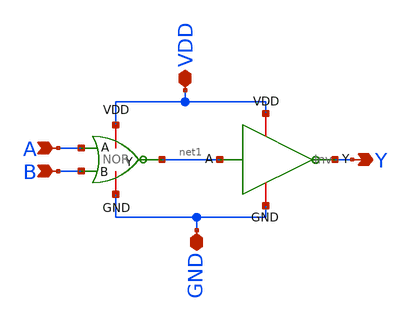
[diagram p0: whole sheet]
** sch_path: FinalProj/OR.sch
**.subckt OR VDD GND A B Y
*.iopin VDD
*.iopin GND
*.ipin A
*.ipin B
*.opin Y
x1 VDD B net1 A GND NOR
x2 VDD net1 Y GND Inv
**.ends

* expanding   symbol:  workspace/FinalProj/NOR.sym # of pins=5
** sym_path: FinalProj/NOR.sym
** sch_path: FinalProj/NOR.sch
.subckt NOR VDD B Y A GND
*.ipin B
*.ipin A
*.iopin GND
*.iopin VDD
*.opin Y
XM1 net1 A VDD VDD sky130_fd_pr__pfet_01v8 L=0.5 W=2 nf=1 ad='int((nf+1)/2) * W/nf * 0.29' as='int((nf+2)/2) * W/nf * 0.29'
+ pd='2*int((nf+1)/2) * (W/nf + 0.29)' ps='2*int((nf+2)/2) * (W/nf + 0.29)' nrd='0.29 / W' nrs='0.29 / W'
+ sa=0 sb=0 sd=0 mult=1 m=1
XM2 Y B net1 VDD sky130_fd_pr__pfet_01v8 L=0.5 W=2 nf=1 ad='int((nf+1)/2) * W/nf * 0.29' as='int((nf+2)/2) * W/nf * 0.29'
+ pd='2*int((nf+1)/2) * (W/nf + 0.29)' ps='2*int((nf+2)/2) * (W/nf + 0.29)' nrd='0.29 / W' nrs='0.29 / W'
+ sa=0 sb=0 sd=0 mult=1 m=1
XM3 Y A GND GND sky130_fd_pr__nfet_01v8 L=0.5 W=0.5 nf=1 ad='int((nf+1)/2) * W/nf * 0.29' as='int((nf+2)/2) * W/nf * 0.29'
+ pd='2*int((nf+1)/2) * (W/nf + 0.29)' ps='2*int((nf+2)/2) * (W/nf + 0.29)' nrd='0.29 / W' nrs='0.29 / W'
+ sa=0 sb=0 sd=0 mult=1 m=1
XM4 Y B GND GND sky130_fd_pr__nfet_01v8 L=0.5 W=0.5 nf=1 ad='int((nf+1)/2) * W/nf * 0.29' as='int((nf+2)/2) * W/nf * 0.29'
+ pd='2*int((nf+1)/2) * (W/nf + 0.29)' ps='2*int((nf+2)/2) * (W/nf + 0.29)' nrd='0.29 / W' nrs='0.29 / W'
+ sa=0 sb=0 sd=0 mult=1 m=1
.ends


* expanding   symbol:  workspace/FinalProj/Inv.sym # of pins=4
** sym_path: FinalProj/Inv.sym
** sch_path: FinalProj/Inv.sch
.subckt Inv VDD A Y GND
*.ipin A
*.iopin GND
*.iopin VDD
*.opin Y
XM1 Y A VDD VDD sky130_fd_pr__pfet_01v8 L=0.5 W=1 nf=1 ad='int((nf+1)/2) * W/nf * 0.29' as='int((nf+2)/2) * W/nf * 0.29'
+ pd='2*int((nf+1)/2) * (W/nf + 0.29)' ps='2*int((nf+2)/2) * (W/nf + 0.29)' nrd='0.29 / W' nrs='0.29 / W'
+ sa=0 sb=0 sd=0 mult=1 m=1
XM2 Y A GND GND sky130_fd_pr__nfet_01v8 L=0.5 W=0.5 nf=1 ad='int((nf+1)/2) * W/nf * 0.29' as='int((nf+2)/2) * W/nf * 0.29'
+ pd='2*int((nf+1)/2) * (W/nf + 0.29)' ps='2*int((nf+2)/2) * (W/nf + 0.29)' nrd='0.29 / W' nrs='0.29 / W'
+ sa=0 sb=0 sd=0 mult=1 m=1
.ends

.end
